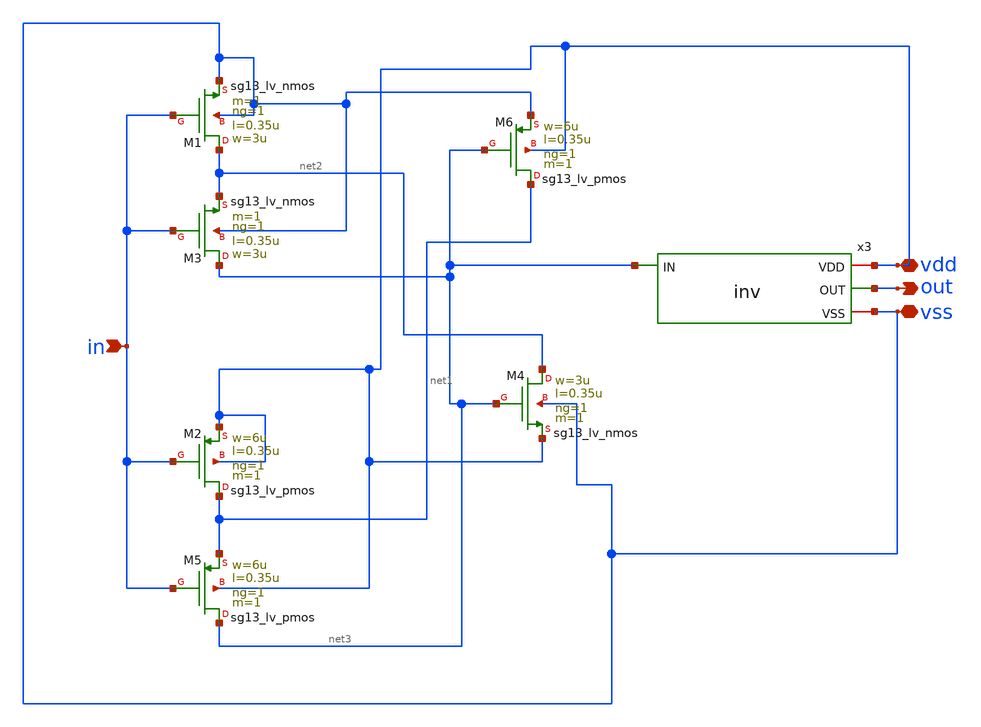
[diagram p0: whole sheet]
** sch_path: macros/heichips26_chronosense/schematic/xschem/schmitt.sch
* macros/heichips26_chronosense/schematic/xschem/inv.sch:
* Copyright 2023 IHP PDK Authors
* Licensed under the Apache License, Version 2.0 (the "License");
**.subckt schmitt in vdd vss out
*.ipin in
*.iopin vdd
*.iopin vss
*.opin out
XM1 net2 in vss vss sg13_lv_nmos w=3u l=0.35u ng=1 m=1 mm_ok=1
XM2 net1 in vdd vdd sg13_lv_pmos w=6u l=0.35u ng=1 m=1 mm_ok=1
XM3 net3 in net2 vss sg13_lv_nmos w=3u l=0.35u ng=1 m=1 mm_ok=1
XM4 net2 net3 vdd vss sg13_lv_nmos w=3u l=0.35u ng=1 m=1 mm_ok=1
XM5 net3 in net1 vdd sg13_lv_pmos w=6u l=0.35u ng=1 m=1 mm_ok=1
XM6 net1 net3 vss vdd sg13_lv_pmos w=6u l=0.35u ng=1 m=1 mm_ok=1
x3 vdd net3 out vss inv
**.ends

* expanding   symbol:
*+  /foss/designs/Hei_Chips/ChronoSense-1/macros/heichips26_chronosense/schematic/xschem/inv.sym # of pins=4
** sym_path: macros/heichips26_chronosense/schematic/xschem/inv.sym
** sch_path: macros/heichips26_chronosense/schematic/xschem/inv.sch
.subckt inv VDD IN OUT VSS
*.ipin IN
*.opin OUT
*.iopin VDD
*.iopin VSS
XM1 OUT IN VDD VDD sg13_lv_pmos w=2u l=0.35u ng=1 m=1 mm_ok=1
XM2 OUT IN VSS VSS sg13_lv_nmos w=1u l=0.35u ng=1 m=1 mm_ok=1
.ends

.end
